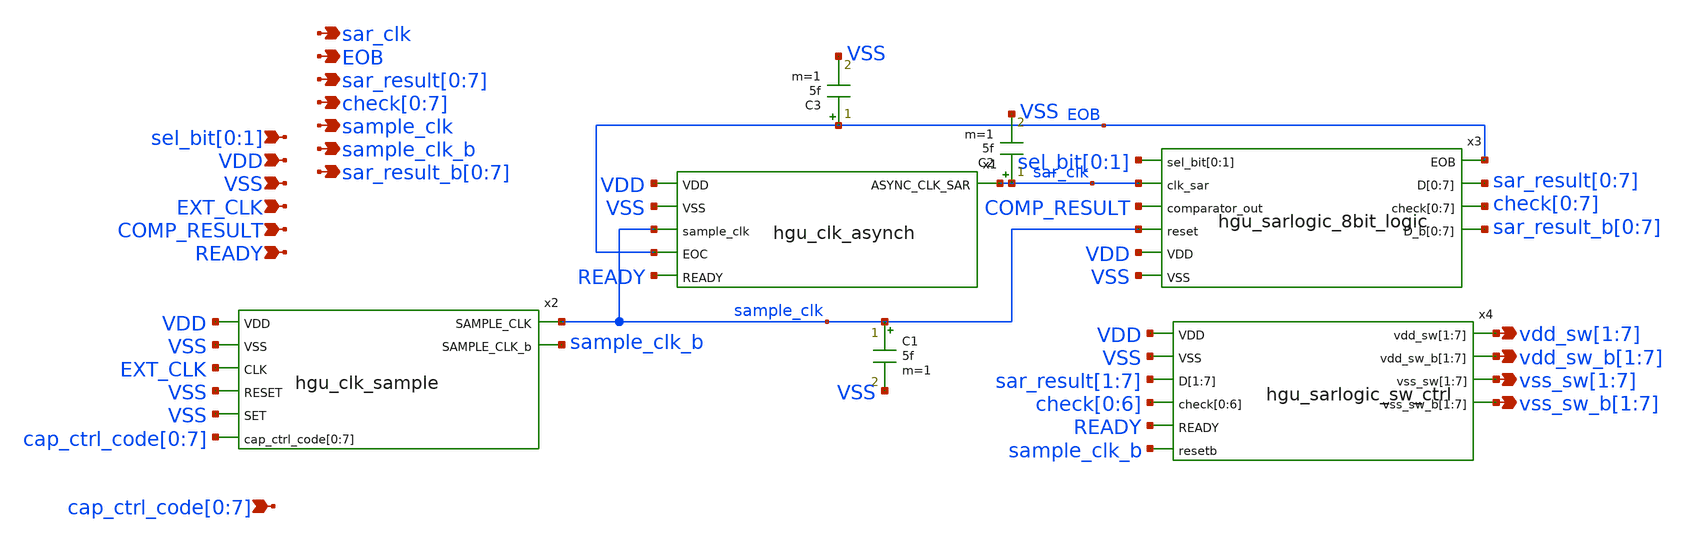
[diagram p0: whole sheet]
** sch_path: hgu/xschem/hgu_sarlogic.sch
**.subckt hgu_sarlogic VDD VSS COMP_RESULT READY EXT_CLK sar_clk EOB
*+ sar_result[0],sar_result[1],sar_result[2],sar_result[3],sar_result[4],sar_result[5],sar_result[6],sar_result[7] check[0],check[1],check[2],check[3],check[4],check[5],check[6],check[7] sample_clk
*+ sel_bit[0],sel_bit[1]
*+ cap_ctrl_code[0],cap_ctrl_code[1],cap_ctrl_code[2],cap_ctrl_code[3],cap_ctrl_code[4],cap_ctrl_code[5],cap_ctrl_code[6],cap_ctrl_code[7] sample_clk_b
*+ sar_result_b[0],sar_result_b[1],sar_result_b[2],sar_result_b[3],sar_result_b[4],sar_result_b[5],sar_result_b[6],sar_result_b[7] vdd_sw[1],vdd_sw[2],vdd_sw[3],vdd_sw[4],vdd_sw[5],vdd_sw[6],vdd_sw[7]
*+ vdd_sw_b[1],vdd_sw_b[2],vdd_sw_b[3],vdd_sw_b[4],vdd_sw_b[5],vdd_sw_b[6],vdd_sw_b[7] vss_sw[1],vss_sw[2],vss_sw[3],vss_sw[4],vss_sw[5],vss_sw[6],vss_sw[7]
*+ vss_sw_b[1],vss_sw_b[2],vss_sw_b[3],vss_sw_b[4],vss_sw_b[5],vss_sw_b[6],vss_sw_b[7]
*.ipin VDD
*.ipin VSS
*.ipin COMP_RESULT
*.ipin READY
*.ipin EXT_CLK
*.opin sar_clk
*.opin EOB
*.opin
*+ sar_result[0],sar_result[1],sar_result[2],sar_result[3],sar_result[4],sar_result[5],sar_result[6],sar_result[7]
*.opin check[0],check[1],check[2],check[3],check[4],check[5],check[6],check[7]
*.opin sample_clk
*.ipin sel_bit[0],sel_bit[1]
*.ipin
*+ cap_ctrl_code[0],cap_ctrl_code[1],cap_ctrl_code[2],cap_ctrl_code[3],cap_ctrl_code[4],cap_ctrl_code[5],cap_ctrl_code[6],cap_ctrl_code[7]
*.opin sample_clk_b
*.opin
*+ sar_result_b[0],sar_result_b[1],sar_result_b[2],sar_result_b[3],sar_result_b[4],sar_result_b[5],sar_result_b[6],sar_result_b[7]
*.opin vdd_sw[1],vdd_sw[2],vdd_sw[3],vdd_sw[4],vdd_sw[5],vdd_sw[6],vdd_sw[7]
*.opin vdd_sw_b[1],vdd_sw_b[2],vdd_sw_b[3],vdd_sw_b[4],vdd_sw_b[5],vdd_sw_b[6],vdd_sw_b[7]
*.opin vss_sw[1],vss_sw[2],vss_sw[3],vss_sw[4],vss_sw[5],vss_sw[6],vss_sw[7]
*.opin vss_sw_b[1],vss_sw_b[2],vss_sw_b[3],vss_sw_b[4],vss_sw_b[5],vss_sw_b[6],vss_sw_b[7]
x1 sar_clk VDD VSS sample_clk EOB READY hgu_clk_asynch
x2 sample_clk VDD VSS EXT_CLK VSS VSS sample_clk_b cap_ctrl_code[0] cap_ctrl_code[1]
+ cap_ctrl_code[2] cap_ctrl_code[3] cap_ctrl_code[4] cap_ctrl_code[5] cap_ctrl_code[6] cap_ctrl_code[7] hgu_clk_sample
x3 sel_bit[0] sel_bit[1] EOB sar_clk sar_result[0] sar_result[1] sar_result[2] sar_result[3]
+ sar_result[4] sar_result[5] sar_result[6] sar_result[7] COMP_RESULT check[0] check[1] check[2] check[3] check[4]
+ check[5] check[6] check[7] sample_clk sar_result_b[0] sar_result_b[1] sar_result_b[2] sar_result_b[3]
+ sar_result_b[4] sar_result_b[5] sar_result_b[6] sar_result_b[7] VDD VSS hgu_sarlogic_8bit_logic csize=0.001
C1 sample_clk VSS 5f m=1
C2 sar_clk VSS 5f m=1
C3 EOB VSS 5f m=1
x4 VDD VSS vdd_sw[1] vdd_sw[2] vdd_sw[3] vdd_sw[4] vdd_sw[5] vdd_sw[6] vdd_sw[7] vdd_sw_b[1]
+ vdd_sw_b[2] vdd_sw_b[3] vdd_sw_b[4] vdd_sw_b[5] vdd_sw_b[6] vdd_sw_b[7] sar_result[1] sar_result[2]
+ sar_result[3] sar_result[4] sar_result[5] sar_result[6] sar_result[7] vss_sw[1] vss_sw[2] vss_sw[3] vss_sw[4]
+ vss_sw[5] vss_sw[6] vss_sw[7] check[0] check[1] check[2] check[3] check[4] check[5] check[6] vss_sw_b[1]
+ vss_sw_b[2] vss_sw_b[3] vss_sw_b[4] vss_sw_b[5] vss_sw_b[6] vss_sw_b[7] READY sample_clk_b hgu_sarlogic_sw_ctrl
**.ends
.end
